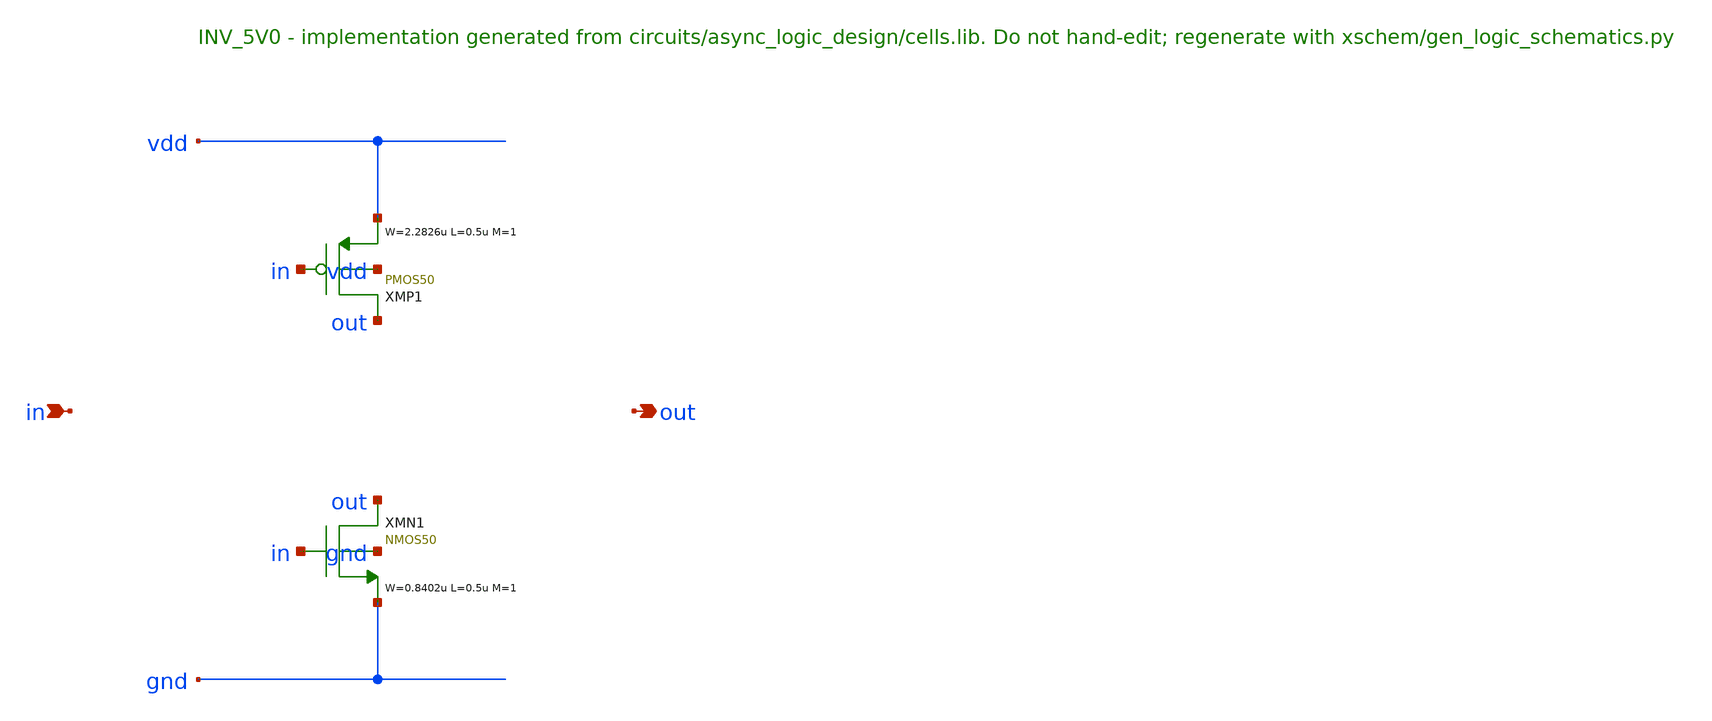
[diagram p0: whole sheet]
** sch_path: xschem/logic/INV_5V0.sch
**.subckt INV_5V0 in out
*.ipin in
*.opin out
XMP1 out in vdd vdd PMOS50 W=2.2826u L=0.5u M=1 MM_SIGMA=0
XMN1 out in gnd gnd NMOS50 W=0.8402u L=0.5u M=1 MM_SIGMA=0
**.ends
.end
